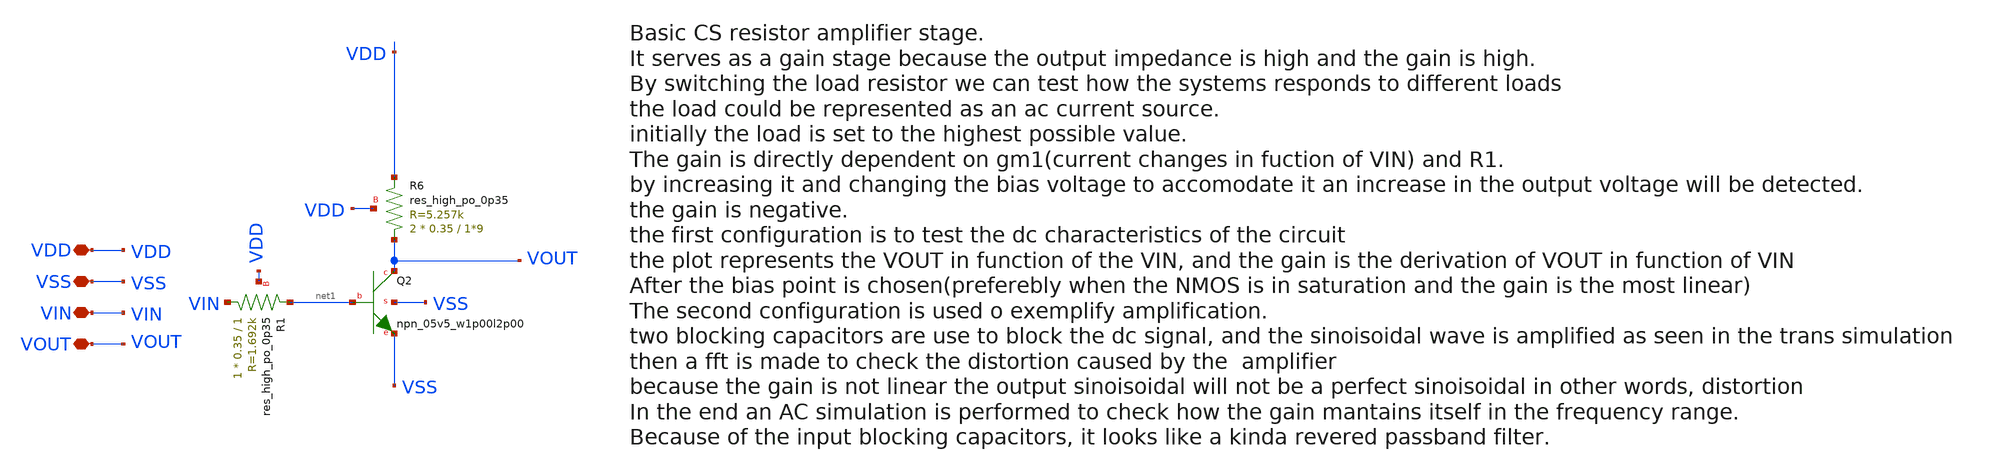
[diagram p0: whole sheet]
** sch_path: old stuff/amplifiers/single_stage_amps/basic_stages/ce_resistive_stage/ce_resistor_stage.sch
**.subckt ce_resistor_stage VDD VSS VIN VOUT
*.iopin VDD
*.iopin VSS
*.iopin VIN
*.iopin VOUT
XR6 VOUT VDD VDD sky130_fd_pr__res_high_po_0p35 L=1*9 mult=2 m=2
XQ2 VOUT net1 VSS VSS sky130_fd_pr__npn_05v5_w1p00l2p00
XR1 VIN net1 VDD sky130_fd_pr__res_high_po_0p35 L=1 mult=1 m=1
**.ends
.end
